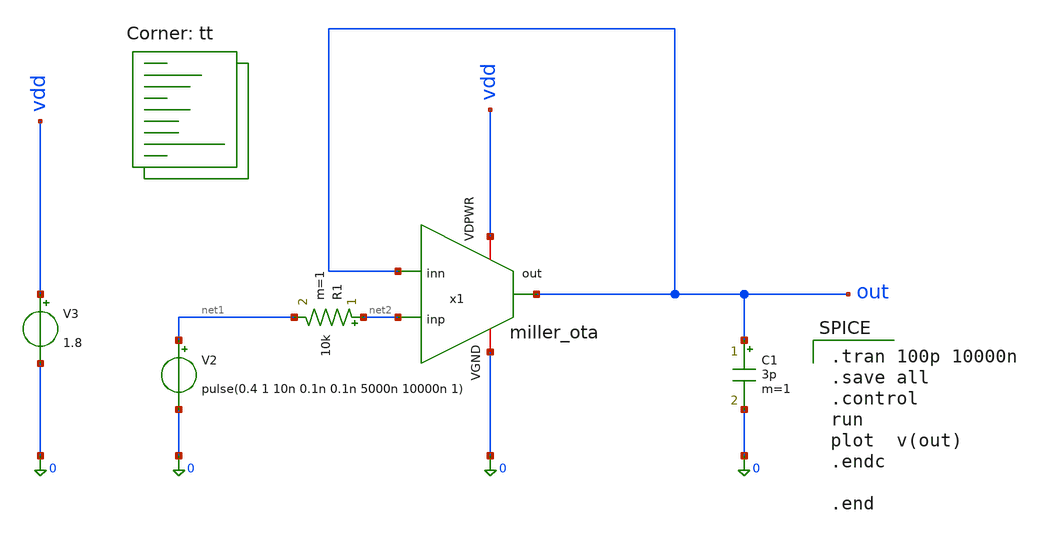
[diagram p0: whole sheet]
** sch_path: src/xschem/miller_ota_test_trans.sch
**.subckt miller_ota_test_trans
x1 vdd out out net2 0 miller_ota
V2 net1 0 pulse(0.4 1 10n 0.1n 0.1n 5000n 10000n 1)
R1 net2 net1 10k m=1
C1 out 0 3p m=1
V3 vdd 0 1.8
**** begin user architecture code

.tran 100p 10000n
.save all
.control
run
plot  v(out)
.endc

.end

.lib $::SKYWATER_MODELS/sky130.lib.spice tt
**** end user architecture code
**.ends
.end
